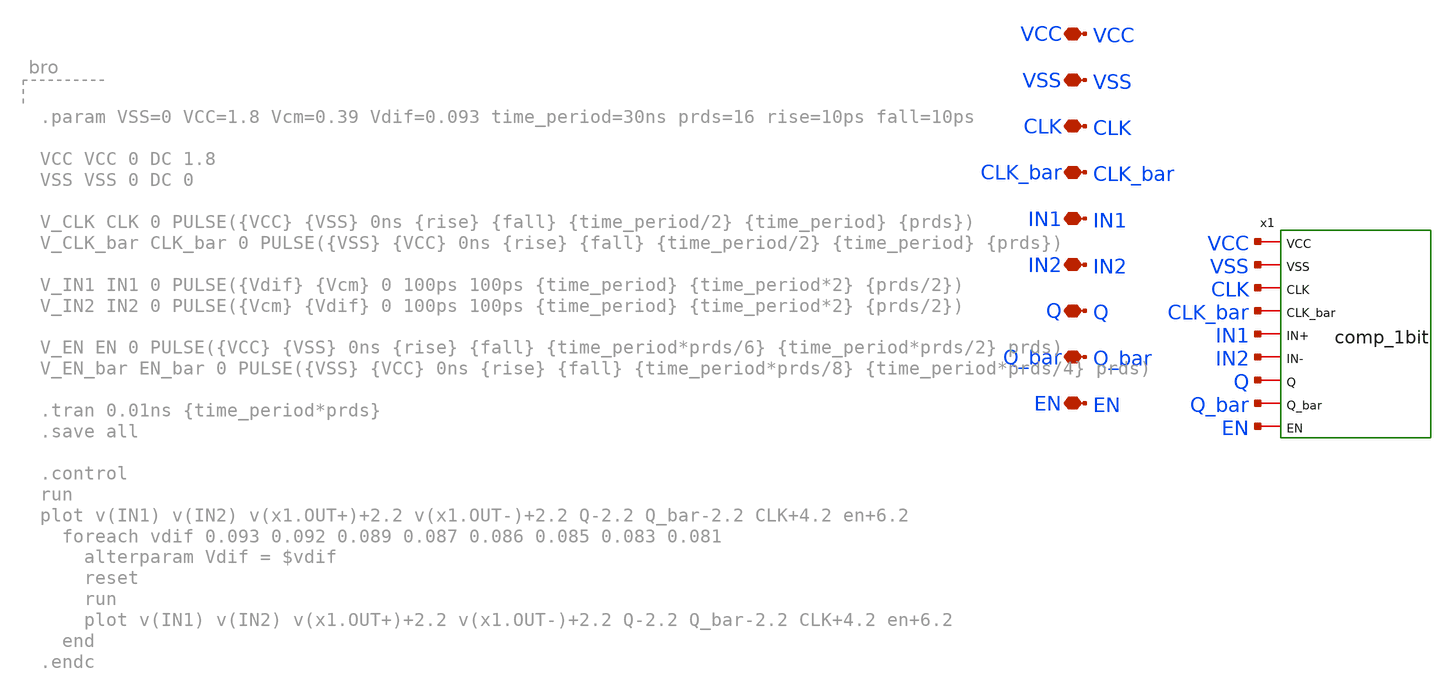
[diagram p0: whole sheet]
** sch_path: voltage_comp/comp_1bit_test.sch
**.subckt comp_1bit_test VSS VCC IN1 IN2 CLK CLK_bar Q Q_bar EN
*.iopin VSS
*.iopin VCC
*.iopin IN1
*.iopin IN2
*.iopin CLK
*.iopin CLK_bar
*.iopin Q
*.iopin Q_bar
*.iopin EN
x1 VCC VSS CLK CLK_bar IN1 IN2 Q Q_bar EN comp_1bit
**** begin user architecture code

** opencircuitdesign pdks install
.lib $::SKYWATER_MODELS/sky130.lib.spice tt



.param VSS=0 VCC=1.8 Vcm=1.45 Vdif=0.3 time_period=30ns prds=130 rise=100ps fall=100ps

VCC VCC 0 DC 1.8
VSS VSS 0 DC 0

V_CLK CLK 0 PULSE({VCC} {VSS} 0ns {rise} {fall} {(time_period)/2} {time_period} {prds})
V_CLK_bar CLK_bar 0 PULSE({VSS} {VCC} 0ns {rise} {fall} {(time_period)/2} {time_period} {prds})

V_EN EN 0 PULSE({VCC} {VSS} 0ns {rise} {fall} {time_period*prds/8} {time_period*prds/4} prds)
V_EN_bar EN_bar 0 PULSE({VSS} {VCC} 0ns {rise} {fall} {time_period*prds/8} {time_period*prds/4} prds)

V_IN1 IN1 0 PWL(0ns 1.897087 7ns 1.897087 14ns 1.897087 21ns 1.897087 28ns 1.897087 35ns 1.897087
+ 42ns 1.897087 49ns 1.897087 56ns 1.897087 63ns 1.897087 69.99ns 1.897087 70ns 1.87899 77ns 1.87899 84ns
+ 1.87899 91ns 1.87899 98ns 1.87899 105ns 1.87899 112ns 1.87899 119ns 1.87899 126ns 1.87899 133ns 1.87899
+ 139.99ns 1.87899 140ns 1.83947 147ns 1.83947 154ns 1.83947 161ns 1.83947 168ns 1.83947 175ns 1.83947 182ns
+ 1.83947 189ns 1.83947 196ns 1.83947 203ns 1.83947 209.99ns 1.83947 210ns 1.757893 217ns 1.757893 224ns
+ 1.757893 231ns 1.757893 238ns 1.757893 245ns 1.757893 252ns 1.757893 259ns 1.757893 266ns 1.757893 273ns
+ 1.757893 279.99ns 1.757893 280ns 1.601119 287ns 1.601119 294ns 1.601119 301ns 1.601119 308ns 1.601119 315ns
+ 1.601119 322ns 1.601119 329ns 1.601119 336ns 1.601119 343ns 1.601119 349.99ns 1.601119 350ns 1.327728 357ns
+ 1.327728 364ns 1.327728 371ns 1.327728 378ns 1.327728 385ns 1.327728 392ns 1.327728 399ns 1.327728 406ns
+ 1.327728 413ns 1.327728 419.99ns 1.327728 420ns 0.900434 427ns 0.900434 434ns 0.900434 441ns 0.900434 448ns
+ 0.900434 455ns 0.900434 462ns 0.900434 469ns 0.900434 476ns 0.900434 483ns 0.900434 489.99ns 0.900434 490ns
+ 0.64 497ns 0.64 504ns 0.64 511ns 0.64 518ns 0.64 525ns 0.64 532ns 0.64 539ns 0.64 546ns 0.64 553ns 0.64)
V_IN2 IN2 0 PWL(0ns 1.902626 6.99ns 1.902626 7ns 1.891547 13.99ns 1.891547 14ns 1.866433 20.99ns
+ 1.866433 21ns 1.812506 27.99ns 1.812506 28ns 1.703279 34.99ns 1.703279 35ns 1.49896 41.99ns 1.49896 42ns
+ 1.156497 48.99ns 1.156497 49ns 0.64437 56ns 0.64437 62.99ns 0.64437 63ns 0.011758 69.99ns 0.011758 70ns
+ 1.902626 76.99ns 1.902626 77ns 1.891547 83.99ns 1.891547 84ns 1.866433 90.99ns 1.866433 91ns 1.812506
+ 97.99ns 1.812506 98ns 1.703279 104.99ns 1.703279 105ns 1.49896 111.99ns 1.49896 112ns 1.156497 118.99ns
+ 1.156497 119ns 0.64437 126ns 0.64437 132.99ns 0.64437 133ns 0.011758 139.99ns 0.011758 140ns 1.902626
+ 146.99ns 1.902626 147ns 1.891547 153.99ns 1.891547 154ns 1.866433 160.99ns 1.866433 161ns 1.812506 167.99ns
+ 1.812506 168ns 1.703279 174.99ns 1.703279 175ns 1.49896 181.99ns 1.49896 182ns 1.156497 188.99ns 1.156497
+ 189ns 0.64437 196ns 0.64437 202.99ns 0.64437 203ns 0.011758 209.99ns 0.011758 210ns 1.902626 216.99ns
+ 1.902626 217ns 1.891547 223.99ns 1.891547 224ns 1.866433 230.99ns 1.866433 231ns 1.812506 237.99ns 1.812506
+ 238ns 1.703279 244.99ns 1.703279 245ns 1.49896 251.99ns 1.49896 252ns 1.156497 258.99ns 1.156497 259ns
+ 0.64437 266ns 0.64437 272.99ns 0.64437 273ns 0.011758 279.99ns 0.011758 280ns 1.902626 286.99ns 1.902626
+ 287ns 1.891547 293.99ns 1.891547 294ns 1.866433 300.99ns 1.866433 301ns 1.812506 307.99ns 1.812506 308ns
+ 1.703279 314.99ns 1.703279 315ns 1.49896 321.99ns 1.49896 322ns 1.156497 328.99ns 1.156497 329ns 0.64437
+ 336ns 0.64437 342.99ns 0.64437 343ns 0.011758 349.99ns 0.011758 350ns 1.902626 356.99ns 1.902626 357ns
+ 1.891547 363.99ns 1.891547 364ns 1.866433 370.99ns 1.866433 371ns 1.812506 377.99ns 1.812506 378ns 1.703279
+ 384.99ns 1.703279 385ns 1.49896 391.99ns 1.49896 392ns 1.156497 398.99ns 1.156497 399ns 0.64437 406ns
+ 0.64437 412.99ns 0.64437 413ns 0.011758 419.99ns 0.011758 420ns 1.902626 426.99ns 1.902626 427ns 1.891547
+ 433.99ns 1.891547 434ns 1.866433 440.99ns 1.866433 441ns 1.812506 447.99ns 1.812506 448ns 1.703279 454.99ns
+ 1.703279 455ns 1.49896 461.99ns 1.49896 462ns 1.156497 468.99ns 1.156497 469ns 0.64437 476ns 0.64437
+ 482.99ns 0.64437 483ns 0.011758 489.99ns 0.011758 490ns 1.902626 496.99ns 1.902626 497ns 1.891547 503.99ns
+ 1.891547 504ns 1.866433 510.99ns 1.866433 511ns 1.812506 517.99ns 1.812506 518ns 1.703279 524.99ns 1.703279
+ 525ns 1.49896 531.99ns 1.49896 532ns 1.156497 538.99ns 1.156497 539ns 0.64437 546ns 0.64437 552.99ns
+ 0.64437 553ns 0.011758)

*V_IN1 IN1 0 PWL(0ns 0.4 30ns 0.4 60ns 0.4 90ns 0.4 120ns 0.4 150ns 0.4 180ns 0.4 210ns 0.4 239.99ns
*+ 0.4 240ns 0.734099 270ns 0.734099 300ns 0.734099 330ns 0.734099 360ns 0.734099 390ns 0.734099 420ns
*+ 0.734099 450ns 0.734099 479.99ns 0.734099 480ns 1.148807 510ns 1.148807 540ns 1.148807 570ns 1.148807 600ns
*+ 1.148807 630ns 1.148807 660ns 1.148807 690ns 1.148807 719.99ns 1.148807 720ns 1.442514 750ns 1.442514 780ns
*+ 1.442514 810ns 1.442514 840ns 1.442514 870ns 1.442514 900ns 1.442514 930ns 1.442514 959.99ns 1.442514 960ns
*+ 1.615965 990ns 1.615965 1020ns 1.615965 1050ns 1.615965 1080ns 1.615965 1110ns 1.615965 1140ns 1.615965
*+ 1170ns 1.615965 1199.99ns 1.615965 1200ns 1.710113 1230ns 1.710113 1260ns 1.710113 1290ns 1.710113 1320ns
*+ 1.710113 1350ns 1.710113 1380ns 1.710113 1410ns 1.710113 1439.99ns 1.710113 1440ns 1.757623 1470ns 1.757623
*+ 1500ns 1.757623 1530ns 1.757623 1560ns 1.757623 1590ns 1.757623 1620ns 1.757623 1650ns 1.757623 1679.99ns
*+ 1.757623 1680ns 1.780524 1710ns 1.780524 1740ns 1.780524 1770ns 1.780524 1800ns 1.780524 1830ns 1.780524
*+ 1860ns 1.780524 1890ns 1.780524)
*V_IN2 IN2 0 PWL(0ns 0.059729 29.99ns 0.059729 30ns 0.501857 59.99ns 0.501857 60ns 0.96634 89.99ns
*+ 0.96634 90ns 1.331275 119.99ns 1.331275 120ns 1.553753 149.99ns 1.553753 150ns 1.678176 179.99ns 1.678176
*+ 180ns 1.773196 209.99ns 1.773196 210ns 1.787852 239.99ns 1.787852 240ns 0.059729 269.99ns 0.059729 270ns
*+ 0.501857 299.99ns 0.501857 300ns 0.96634 329.99ns 0.96634 330ns 1.331275 359.99ns 1.331275 360ns 1.553753
*+ 389.99ns 1.553753 390ns 1.678176 419.99ns 1.678176 420ns 1.773196 449.99ns 1.773196 450ns 1.787852 479.99ns
*+ 1.787852 480ns 0.059729 509.99ns 0.059729 510ns 0.501857 539.99ns 0.501857 540ns 0.96634 569.99ns 0.96634
*+ 570ns 1.331275 599.99ns 1.331275 600ns 1.553753 629.99ns 1.553753 630ns 1.678176 659.99ns 1.678176 660ns
*+ 1.773196 689.99ns 1.773196 690ns 1.787852 719.99ns 1.787852 720ns 0.059729 749.99ns 0.059729 750ns 0.501857
*+ 779.99ns 0.501857 780ns 0.96634 809.99ns 0.96634 810ns 1.331275 839.99ns 1.331275 840ns 1.553753 869.99ns
*+ 1.553753 870ns 1.678176 899.99ns 1.678176 900ns 1.773196 929.99ns 1.773196 930ns 1.787852 959.99ns 1.787852
*+ 960ns 0.059729 989.99ns 0.059729 990ns 0.501857 1019.99ns 0.501857 1020ns 0.96634 1049.99ns 0.96634
*+ 1050ns 1.331275 1079.99ns 1.331275 1080ns 1.553753 1109.99ns 1.553753 1110ns 1.678176 1139.99ns 1.678176
*+ 1140ns 1.773196 1169.99ns 1.773196 1170ns 1.787852 1199.99ns 1.787852 1200ns 0.059729 1229.99ns 0.059729
*+ 1230ns 0.501857 1259.99ns 0.501857 1260ns 0.96634 1289.99ns 0.96634 1290ns 1.331275 1319.99ns 1.331275
*+ 1320ns 1.553753 1349.99ns 1.553753 1350ns 1.678176 1379.99ns 1.678176 1380ns 1.773196 1409.99ns 1.773196
*+ 1410ns 1.787852 1439.99ns 1.787852 1440ns 0.059729 1469.99ns 0.059729 1470ns 0.501857 1499.99ns 0.501857
*+ 1500ns 0.96634 1529.99ns 0.96634 1530ns 1.331275 1559.99ns 1.331275 1560ns 1.553753 1589.99ns 1.553753
*+ 1590ns 1.678176 1619.99ns 1.678176 1620ns 1.773196 1649.99ns 1.773196 1650ns 1.787852 1679.99ns 1.787852
*+ 1680ns 0.059729 1709.99ns 0.059729 1710ns 0.501857 1739.99ns 0.501857 1740ns 0.96634 1769.99ns 0.96634
*+ 1770ns 1.331275 1799.99ns 1.331275 1800ns 1.553753 1829.99ns 1.553753 1830ns 1.678176 1859.99ns 1.678176
*+ 1860ns 1.773196 1889.99ns 1.773196 1890ns 1.787852)

.tran 0.01ns 3840ns
.save all

.control
run
plot v(IN1)+2.2 v(IN2)+2.2 v(x1.OUT+) v(x1.OUT-) Q-2.2 CLK+4.4
.endc


**** end user architecture code
**.ends
.end
